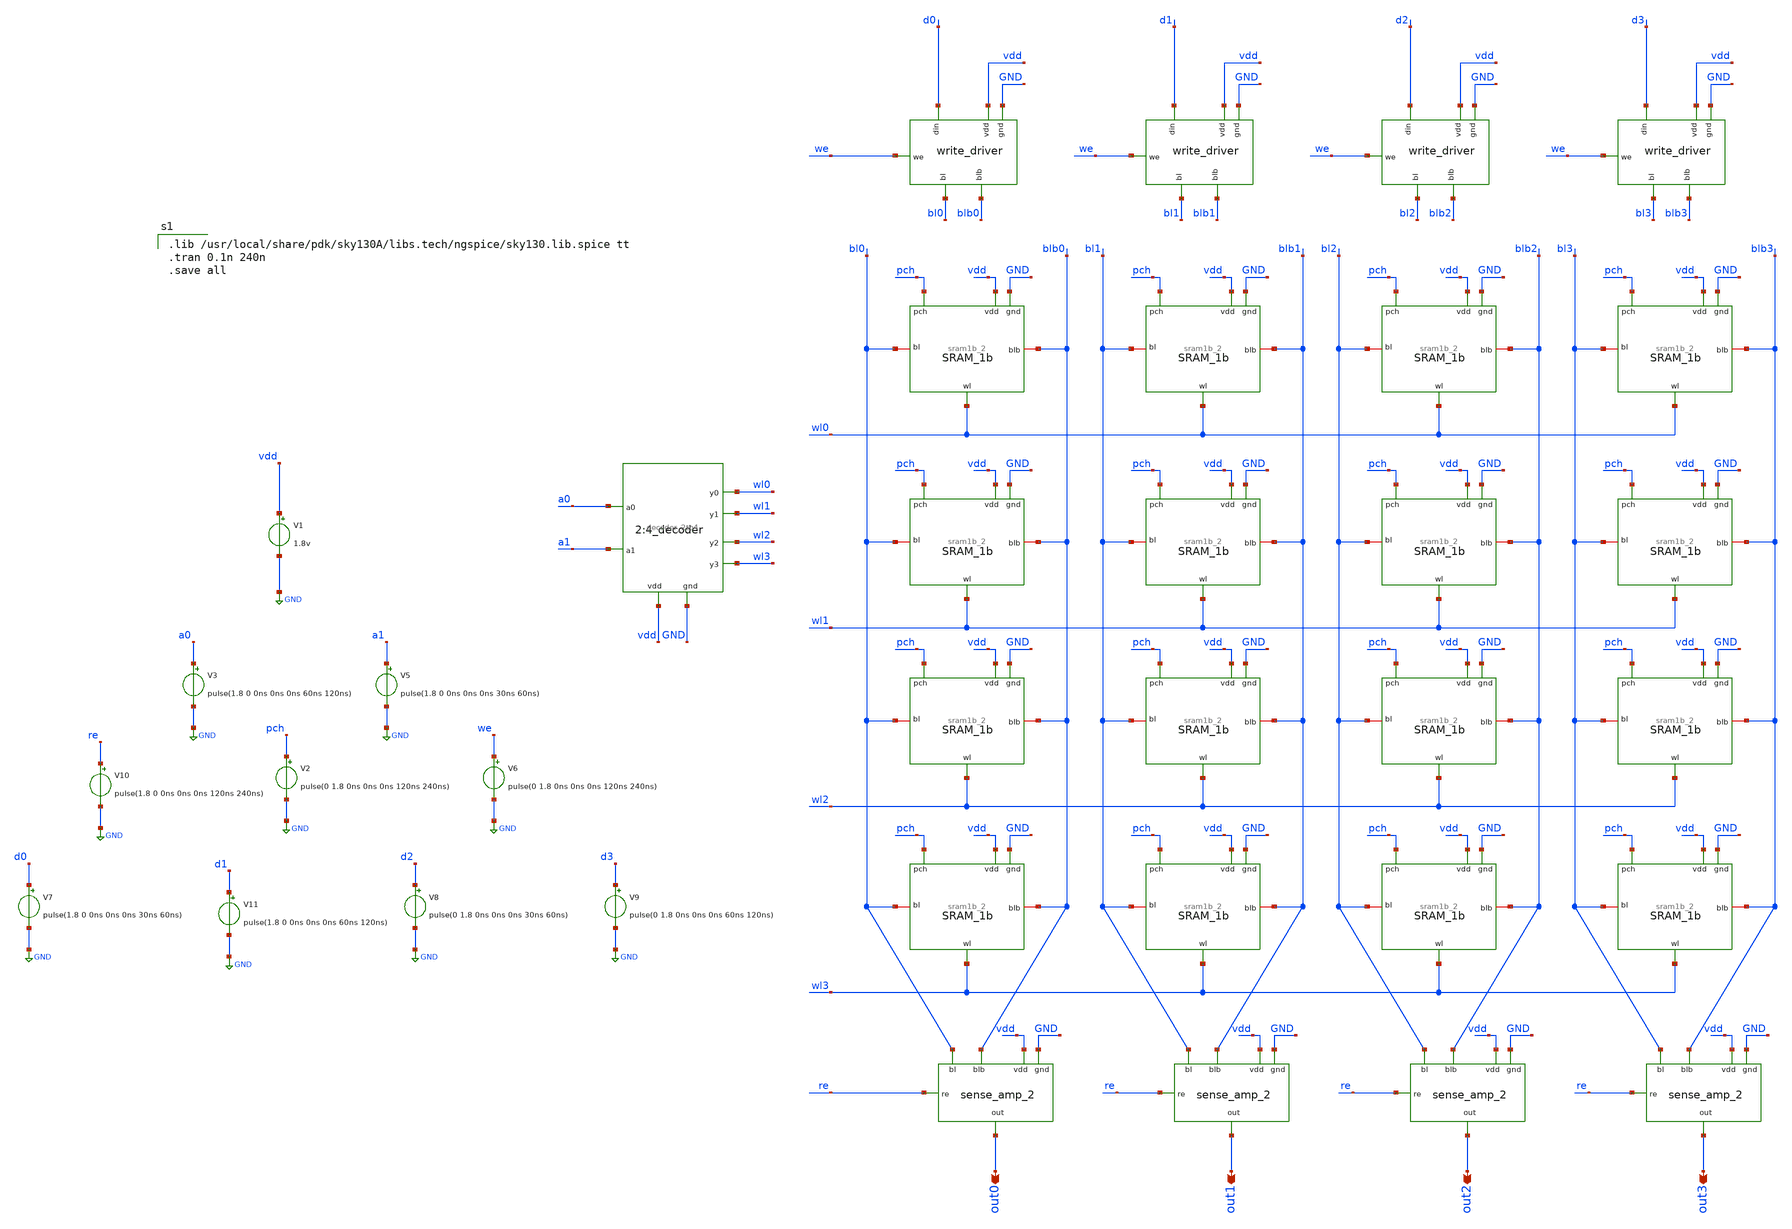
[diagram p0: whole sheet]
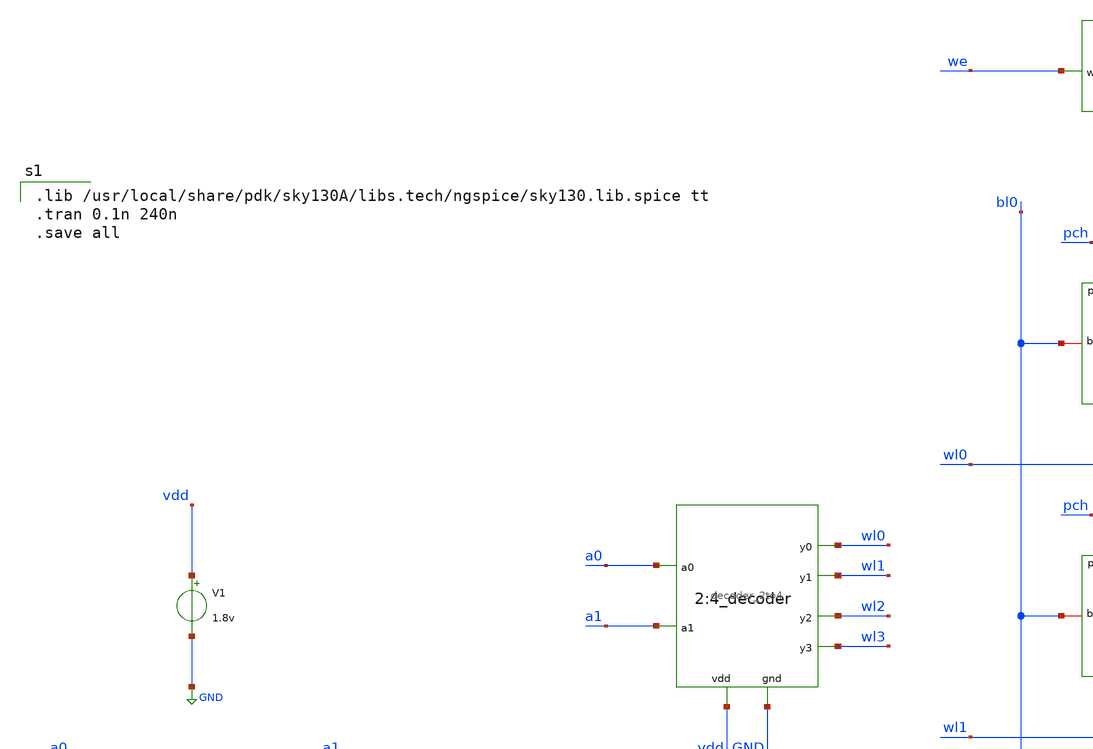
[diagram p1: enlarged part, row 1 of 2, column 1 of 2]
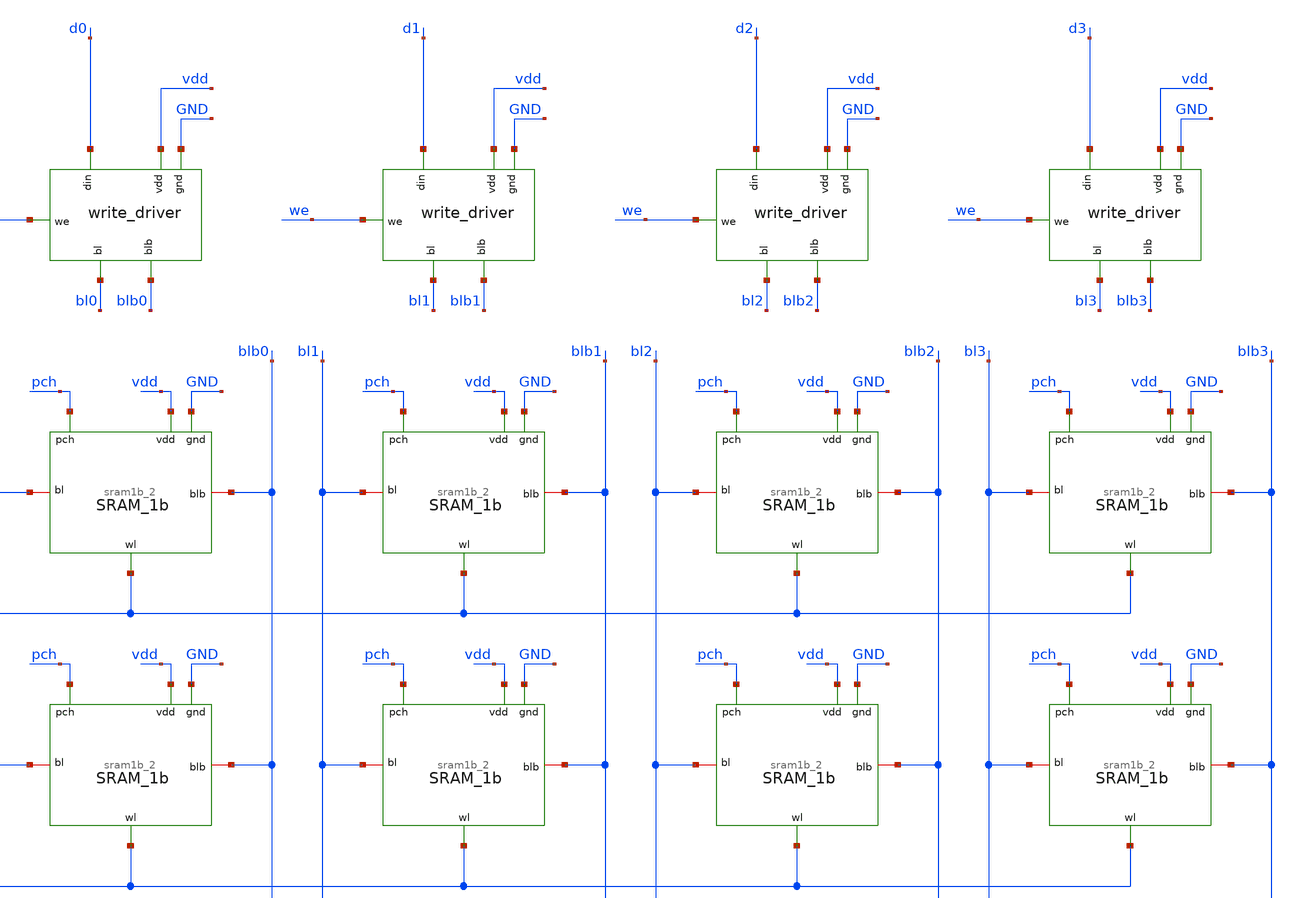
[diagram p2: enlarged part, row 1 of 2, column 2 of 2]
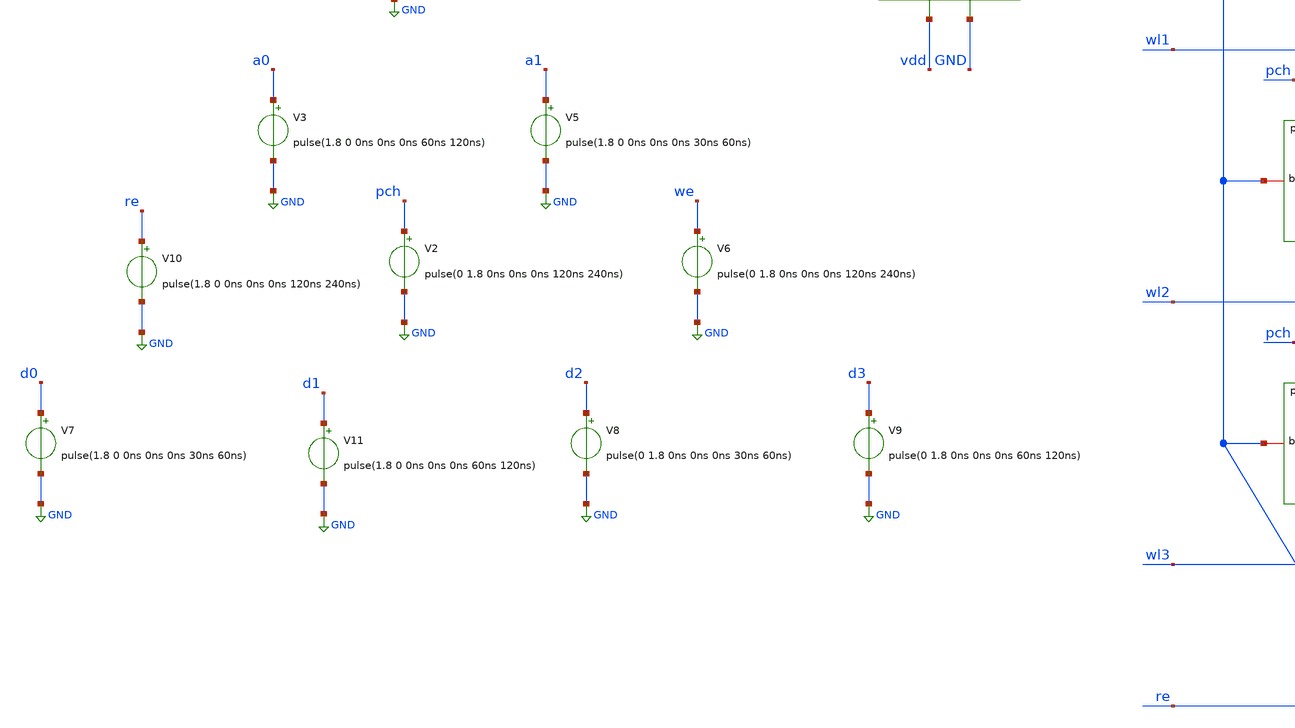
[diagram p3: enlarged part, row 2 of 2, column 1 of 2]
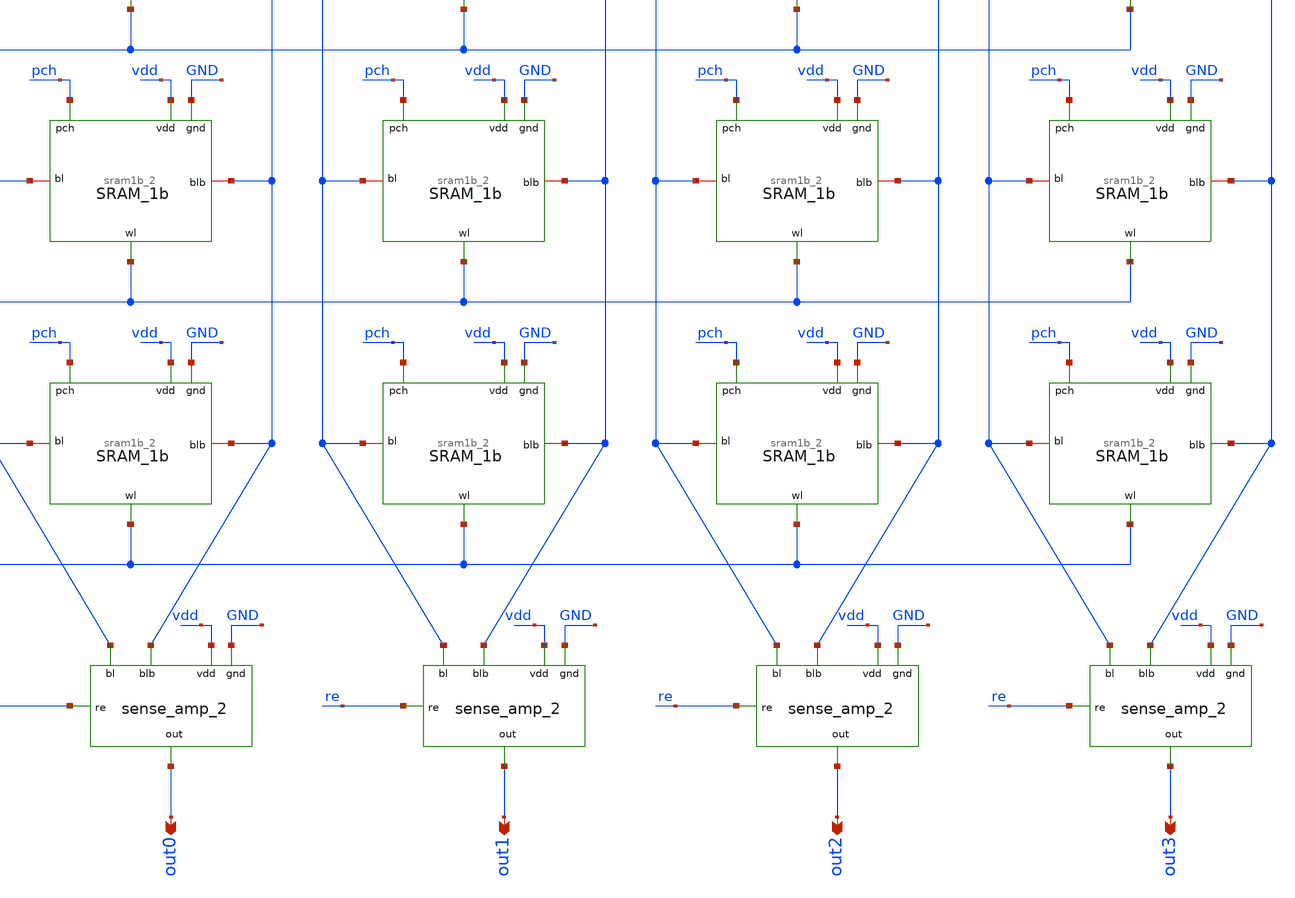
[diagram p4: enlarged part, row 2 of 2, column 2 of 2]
** sch_path: sram/4x4_sram.sch
**.subckt 4x4_sram out0 out1 out2 out3
*.opin out0
*.opin out1
*.opin out2
*.opin out3
x1 pch wl0 vdd bl0 blb0 GND sram1b_2
x2 wl0 vdd GND a0 a1 wl1 wl2 wl3 decoder_2to4
x3 vdd GND d0 bl0 blb0 we write_driver
x6 pch wl0 vdd bl1 blb1 GND sram1b_2
x7 pch wl0 vdd bl2 blb2 GND sram1b_2
x8 pch wl0 vdd bl3 blb3 GND sram1b_2
x9 pch wl1 vdd bl0 blb0 GND sram1b_2
x10 pch wl1 vdd bl1 blb1 GND sram1b_2
x11 pch wl1 vdd bl2 blb2 GND sram1b_2
x12 pch wl1 vdd bl3 blb3 GND sram1b_2
x13 pch wl2 vdd bl0 blb0 GND sram1b_2
x14 pch wl2 vdd bl1 blb1 GND sram1b_2
x15 pch wl2 vdd bl2 blb2 GND sram1b_2
x16 pch wl2 vdd bl3 blb3 GND sram1b_2
x17 pch wl3 vdd bl0 blb0 GND sram1b_2
x18 pch wl3 vdd bl1 blb1 GND sram1b_2
x19 pch wl3 vdd bl2 blb2 GND sram1b_2
x20 pch wl3 vdd bl3 blb3 GND sram1b_2
x21 vdd GND d1 bl1 blb1 we write_driver
x22 vdd GND d2 bl2 blb2 we write_driver
x23 vdd GND d3 bl3 blb3 we write_driver
V1 vdd GND 1.8v
V3 a0 GND pulse(1.8 0 0ns 0ns 0ns 60ns 120ns)
V2 pch GND pulse(0 1.8 0ns 0ns 0ns 120ns 240ns)
V5 a1 GND pulse(1.8 0 0ns 0ns 0ns 30ns 60ns)
V6 we GND pulse(0 1.8 0ns 0ns 0ns 120ns 240ns)
V7 d0 GND pulse(1.8 0 0ns 0ns 0ns 30ns 60ns)
V11 d1 GND pulse(1.8 0 0ns 0ns 0ns 60ns 120ns)
V8 d2 GND pulse(0 1.8 0ns 0ns 0ns 30ns 60ns)
V9 d3 GND pulse(0 1.8 0ns 0ns 0ns 60ns 120ns)
V10 re GND pulse(1.8 0 0ns 0ns 0ns 120ns 240ns)
x4 vdd out0 bl0 blb0 re GND sense_amp_2
x5 vdd out1 bl1 blb1 re GND sense_amp_2
x24 vdd out2 bl2 blb2 re GND sense_amp_2
x25 vdd out3 bl3 blb3 re GND sense_amp_2
**** begin user architecture code

.lib /usr/local/share/pdk/sky130A/libs.tech/ngspice/sky130.lib.spice tt
.tran 0.1n 240n
.save all

**** end user architecture code
**.ends

* expanding   symbol:  sram1b_2.sym # of pins=6
** sym_path: sram/sram1b_2.sym
** sch_path: sram/sram1b_2.sch
.subckt sram1b_2 pch wl vdd bl blb gnd
*.ipin gnd
*.ipin vdd
*.ipin wl
*.ipin pch
*.iopin blb
*.iopin bl
XM1 blb wl net2 gnd sky130_fd_pr__nfet_01v8 L=0.15 W=1 nf=1 ad='int((nf+1)/2) * W/nf * 0.29' as='int((nf+2)/2) * W/nf * 0.29'
+ pd='2*int((nf+1)/2) * (W/nf + 0.29)' ps='2*int((nf+2)/2) * (W/nf + 0.29)' nrd='0.29 / W' nrs='0.29 / W'
+ sa=0 sb=0 sd=0 mult=1 m=1
XM3 net1 wl bl gnd sky130_fd_pr__nfet_01v8 L=0.15 W=1 nf=1 ad='int((nf+1)/2) * W/nf * 0.29' as='int((nf+2)/2) * W/nf * 0.29'
+ pd='2*int((nf+1)/2) * (W/nf + 0.29)' ps='2*int((nf+2)/2) * (W/nf + 0.29)' nrd='0.29 / W' nrs='0.29 / W'
+ sa=0 sb=0 sd=0 mult=1 m=1
XM5 net1 net2 vdd vdd sky130_fd_pr__pfet_01v8 L=0.15 W=1 nf=1 ad='int((nf+1)/2) * W/nf * 0.29' as='int((nf+2)/2) * W/nf * 0.29'
+ pd='2*int((nf+1)/2) * (W/nf + 0.29)' ps='2*int((nf+2)/2) * (W/nf + 0.29)' nrd='0.29 / W' nrs='0.29 / W'
+ sa=0 sb=0 sd=0 mult=1 m=1
XM6 net2 net1 vdd vdd sky130_fd_pr__pfet_01v8 L=0.15 W=1 nf=1 ad='int((nf+1)/2) * W/nf * 0.29' as='int((nf+2)/2) * W/nf * 0.29'
+ pd='2*int((nf+1)/2) * (W/nf + 0.29)' ps='2*int((nf+2)/2) * (W/nf + 0.29)' nrd='0.29 / W' nrs='0.29 / W'
+ sa=0 sb=0 sd=0 mult=1 m=1
XM7 bl pch vdd vdd sky130_fd_pr__pfet_01v8 L=0.15 W=1 nf=1 ad='int((nf+1)/2) * W/nf * 0.29' as='int((nf+2)/2) * W/nf * 0.29'
+ pd='2*int((nf+1)/2) * (W/nf + 0.29)' ps='2*int((nf+2)/2) * (W/nf + 0.29)' nrd='0.29 / W' nrs='0.29 / W'
+ sa=0 sb=0 sd=0 mult=1 m=1
XM8 blb pch vdd vdd sky130_fd_pr__pfet_01v8 L=0.15 W=1 nf=1 ad='int((nf+1)/2) * W/nf * 0.29' as='int((nf+2)/2) * W/nf * 0.29'
+ pd='2*int((nf+1)/2) * (W/nf + 0.29)' ps='2*int((nf+2)/2) * (W/nf + 0.29)' nrd='0.29 / W' nrs='0.29 / W'
+ sa=0 sb=0 sd=0 mult=1 m=1
XM9 bl pch blb blb sky130_fd_pr__pfet_01v8 L=0.15 W=1 nf=1 ad='int((nf+1)/2) * W/nf * 0.29' as='int((nf+2)/2) * W/nf * 0.29'
+ pd='2*int((nf+1)/2) * (W/nf + 0.29)' ps='2*int((nf+2)/2) * (W/nf + 0.29)' nrd='0.29 / W' nrs='0.29 / W'
+ sa=0 sb=0 sd=0 mult=1 m=1
XM2 net2 net1 gnd gnd sky130_fd_pr__nfet_01v8 L=0.15 W=1 nf=1 ad='int((nf+1)/2) * W/nf * 0.29' as='int((nf+2)/2) * W/nf * 0.29'
+ pd='2*int((nf+1)/2) * (W/nf + 0.29)' ps='2*int((nf+2)/2) * (W/nf + 0.29)' nrd='0.29 / W' nrs='0.29 / W'
+ sa=0 sb=0 sd=0 mult=1 m=1
XM4 net1 net2 gnd gnd sky130_fd_pr__nfet_01v8 L=0.15 W=1 nf=1 ad='int((nf+1)/2) * W/nf * 0.29' as='int((nf+2)/2) * W/nf * 0.29'
+ pd='2*int((nf+1)/2) * (W/nf + 0.29)' ps='2*int((nf+2)/2) * (W/nf + 0.29)' nrd='0.29 / W' nrs='0.29 / W'
+ sa=0 sb=0 sd=0 mult=1 m=1
.ends


* expanding   symbol:  decoder_2to4.sym # of pins=8
** sym_path: sram/decoder_2to4.sym
** sch_path: sram/decoder_2to4.sch
.subckt decoder_2to4 y0 vdd gnd a0 a1 y1 y2 y3
*.opin y0
*.opin y1
*.opin y2
*.opin y3
*.ipin vdd
*.ipin gnd
*.ipin a0
*.ipin a1
x1 vdd a0b y0 a1b gnd and_gate
x2 vdd a0 a0b gnd inverter
x3 vdd a0b y1 a1 gnd and_gate
x4 vdd a0 y2 a1b gnd and_gate
x5 vdd a0 y3 a1 gnd and_gate
x6 vdd a1 a1b gnd inverter
.ends


* expanding   symbol:  write_driver.sym # of pins=6
** sym_path: sram/write_driver.sym
** sch_path: sram/write_driver.sch
.subckt write_driver vdd gnd din bl blb we
*.ipin din
*.ipin we
*.opin bl
*.opin blb
*.ipin vdd
*.ipin gnd
XM1 net2 web vdd vdd sky130_fd_pr__pfet_01v8 L=0.15 W=1 nf=1 ad='int((nf+1)/2) * W/nf * 0.29' as='int((nf+2)/2) * W/nf * 0.29'
+ pd='2*int((nf+1)/2) * (W/nf + 0.29)' ps='2*int((nf+2)/2) * (W/nf + 0.29)' nrd='0.29 / W' nrs='0.29 / W'
+ sa=0 sb=0 sd=0 mult=1 m=1
XM2 blb din net1 blb sky130_fd_pr__nfet_01v8 L=0.15 W=1 nf=1 ad='int((nf+1)/2) * W/nf * 0.29' as='int((nf+2)/2) * W/nf * 0.29'
+ pd='2*int((nf+1)/2) * (W/nf + 0.29)' ps='2*int((nf+2)/2) * (W/nf + 0.29)' nrd='0.29 / W' nrs='0.29 / W'
+ sa=0 sb=0 sd=0 mult=1 m=1
XM3 blb din net2 net2 sky130_fd_pr__pfet_01v8 L=0.15 W=1 nf=1 ad='int((nf+1)/2) * W/nf * 0.29' as='int((nf+2)/2) * W/nf * 0.29'
+ pd='2*int((nf+1)/2) * (W/nf + 0.29)' ps='2*int((nf+2)/2) * (W/nf + 0.29)' nrd='0.29 / W' nrs='0.29 / W'
+ sa=0 sb=0 sd=0 mult=1 m=1
XM4 net1 we gnd net1 sky130_fd_pr__nfet_01v8 L=0.15 W=1 nf=1 ad='int((nf+1)/2) * W/nf * 0.29' as='int((nf+2)/2) * W/nf * 0.29'
+ pd='2*int((nf+1)/2) * (W/nf + 0.29)' ps='2*int((nf+2)/2) * (W/nf + 0.29)' nrd='0.29 / W' nrs='0.29 / W'
+ sa=0 sb=0 sd=0 mult=1 m=1
XM5 net4 web vdd vdd sky130_fd_pr__pfet_01v8 L=0.15 W=1 nf=1 ad='int((nf+1)/2) * W/nf * 0.29' as='int((nf+2)/2) * W/nf * 0.29'
+ pd='2*int((nf+1)/2) * (W/nf + 0.29)' ps='2*int((nf+2)/2) * (W/nf + 0.29)' nrd='0.29 / W' nrs='0.29 / W'
+ sa=0 sb=0 sd=0 mult=1 m=1
XM6 bl dinb net3 net3 sky130_fd_pr__nfet_01v8 L=0.15 W=1 nf=1 ad='int((nf+1)/2) * W/nf * 0.29' as='int((nf+2)/2) * W/nf * 0.29'
+ pd='2*int((nf+1)/2) * (W/nf + 0.29)' ps='2*int((nf+2)/2) * (W/nf + 0.29)' nrd='0.29 / W' nrs='0.29 / W'
+ sa=0 sb=0 sd=0 mult=1 m=1
XM7 bl dinb net4 net4 sky130_fd_pr__pfet_01v8 L=0.15 W=1 nf=1 ad='int((nf+1)/2) * W/nf * 0.29' as='int((nf+2)/2) * W/nf * 0.29'
+ pd='2*int((nf+1)/2) * (W/nf + 0.29)' ps='2*int((nf+2)/2) * (W/nf + 0.29)' nrd='0.29 / W' nrs='0.29 / W'
+ sa=0 sb=0 sd=0 mult=1 m=1
XM8 net3 we gnd gnd sky130_fd_pr__nfet_01v8 L=0.15 W=1 nf=1 ad='int((nf+1)/2) * W/nf * 0.29' as='int((nf+2)/2) * W/nf * 0.29'
+ pd='2*int((nf+1)/2) * (W/nf + 0.29)' ps='2*int((nf+2)/2) * (W/nf + 0.29)' nrd='0.29 / W' nrs='0.29 / W'
+ sa=0 sb=0 sd=0 mult=1 m=1
x1 vdd din dinb gnd inverter
x2 vdd we web gnd inverter
.ends


* expanding   symbol:  sense_amp_2.sym # of pins=6
** sym_path: sram/sense_amp_2.sym
** sch_path: sram/sense_amp_2.sch
.subckt sense_amp_2 vdd out bl blb re gnd
*.ipin gnd
*.ipin vdd
*.ipin re
*.ipin bl
*.ipin blb
*.opin out
XM5 net1 net1 vdd vdd sky130_fd_pr__pfet_01v8 L=0.15 W=1 nf=1 ad='int((nf+1)/2) * W/nf * 0.29' as='int((nf+2)/2) * W/nf * 0.29'
+ pd='2*int((nf+1)/2) * (W/nf + 0.29)' ps='2*int((nf+2)/2) * (W/nf + 0.29)' nrd='0.29 / W' nrs='0.29 / W'
+ sa=0 sb=0 sd=0 mult=1 m=1
XM6 out net1 vdd vdd sky130_fd_pr__pfet_01v8 L=0.15 W=1 nf=1 ad='int((nf+1)/2) * W/nf * 0.29' as='int((nf+2)/2) * W/nf * 0.29'
+ pd='2*int((nf+1)/2) * (W/nf + 0.29)' ps='2*int((nf+2)/2) * (W/nf + 0.29)' nrd='0.29 / W' nrs='0.29 / W'
+ sa=0 sb=0 sd=0 mult=1 m=1
XM2 out blb net2 gnd sky130_fd_pr__nfet_01v8 L=0.15 W=1 nf=1 ad='int((nf+1)/2) * W/nf * 0.29' as='int((nf+2)/2) * W/nf * 0.29'
+ pd='2*int((nf+1)/2) * (W/nf + 0.29)' ps='2*int((nf+2)/2) * (W/nf + 0.29)' nrd='0.29 / W' nrs='0.29 / W'
+ sa=0 sb=0 sd=0 mult=1 m=1
XM4 net1 bl net2 gnd sky130_fd_pr__nfet_01v8 L=0.15 W=1 nf=1 ad='int((nf+1)/2) * W/nf * 0.29' as='int((nf+2)/2) * W/nf * 0.29'
+ pd='2*int((nf+1)/2) * (W/nf + 0.29)' ps='2*int((nf+2)/2) * (W/nf + 0.29)' nrd='0.29 / W' nrs='0.29 / W'
+ sa=0 sb=0 sd=0 mult=1 m=1
XM1 net2 re gnd gnd sky130_fd_pr__nfet_01v8 L=0.15 W=1 nf=1 ad='int((nf+1)/2) * W/nf * 0.29' as='int((nf+2)/2) * W/nf * 0.29'
+ pd='2*int((nf+1)/2) * (W/nf + 0.29)' ps='2*int((nf+2)/2) * (W/nf + 0.29)' nrd='0.29 / W' nrs='0.29 / W'
+ sa=0 sb=0 sd=0 mult=1 m=1
.ends


* expanding   symbol:  and_gate.sym # of pins=5
** sym_path: sram/and_gate.sym
** sch_path: sram/and_gate.sch
.subckt and_gate vdd a y b gnd
*.ipin a
*.ipin b
*.ipin vdd
*.ipin gnd
*.opin y
x2 vdd net1 y gnd inverter
x1 vdd a b gnd net1 nand_gate
.ends


* expanding   symbol:  inverter.sym # of pins=4
** sym_path: sram/inverter.sym
** sch_path: sram/inverter.sch
.subckt inverter vdd vin vout gnd
*.ipin vin
*.ipin vdd
*.ipin gnd
*.opin vout
XM1 vout vin gnd gnd sky130_fd_pr__nfet_01v8 L=0.15 W=1 nf=1 ad='int((nf+1)/2) * W/nf * 0.29' as='int((nf+2)/2) * W/nf * 0.29'
+ pd='2*int((nf+1)/2) * (W/nf + 0.29)' ps='2*int((nf+2)/2) * (W/nf + 0.29)' nrd='0.29 / W' nrs='0.29 / W'
+ sa=0 sb=0 sd=0 mult=1 m=1
XM2 vout vin vdd vdd sky130_fd_pr__pfet_01v8 L=0.15 W=1 nf=1 ad='int((nf+1)/2) * W/nf * 0.29' as='int((nf+2)/2) * W/nf * 0.29'
+ pd='2*int((nf+1)/2) * (W/nf + 0.29)' ps='2*int((nf+2)/2) * (W/nf + 0.29)' nrd='0.29 / W' nrs='0.29 / W'
+ sa=0 sb=0 sd=0 mult=1 m=1
.ends


* expanding   symbol:  nand_gate.sym # of pins=5
** sym_path: sram/nand_gate.sym
** sch_path: sram/nand_gate.sch
.subckt nand_gate vdd a b gnd y
*.ipin a
*.ipin b
*.ipin vdd
*.ipin gnd
*.opin y
XM1 y a vdd vdd sky130_fd_pr__pfet_01v8 L=0.15 W=1 nf=1 ad='int((nf+1)/2) * W/nf * 0.29' as='int((nf+2)/2) * W/nf * 0.29'
+ pd='2*int((nf+1)/2) * (W/nf + 0.29)' ps='2*int((nf+2)/2) * (W/nf + 0.29)' nrd='0.29 / W' nrs='0.29 / W'
+ sa=0 sb=0 sd=0 mult=1 m=1
XM2 y a net1 net1 sky130_fd_pr__nfet_01v8 L=0.15 W=1 nf=1 ad='int((nf+1)/2) * W/nf * 0.29' as='int((nf+2)/2) * W/nf * 0.29'
+ pd='2*int((nf+1)/2) * (W/nf + 0.29)' ps='2*int((nf+2)/2) * (W/nf + 0.29)' nrd='0.29 / W' nrs='0.29 / W'
+ sa=0 sb=0 sd=0 mult=1 m=1
XM3 y b vdd vdd sky130_fd_pr__pfet_01v8 L=0.15 W=1 nf=1 ad='int((nf+1)/2) * W/nf * 0.29' as='int((nf+2)/2) * W/nf * 0.29'
+ pd='2*int((nf+1)/2) * (W/nf + 0.29)' ps='2*int((nf+2)/2) * (W/nf + 0.29)' nrd='0.29 / W' nrs='0.29 / W'
+ sa=0 sb=0 sd=0 mult=1 m=1
XM4 net1 b gnd gnd sky130_fd_pr__nfet_01v8 L=0.15 W=1 nf=1 ad='int((nf+1)/2) * W/nf * 0.29' as='int((nf+2)/2) * W/nf * 0.29'
+ pd='2*int((nf+1)/2) * (W/nf + 0.29)' ps='2*int((nf+2)/2) * (W/nf + 0.29)' nrd='0.29 / W' nrs='0.29 / W'
+ sa=0 sb=0 sd=0 mult=1 m=1
.ends

.GLOBAL GND
.end
